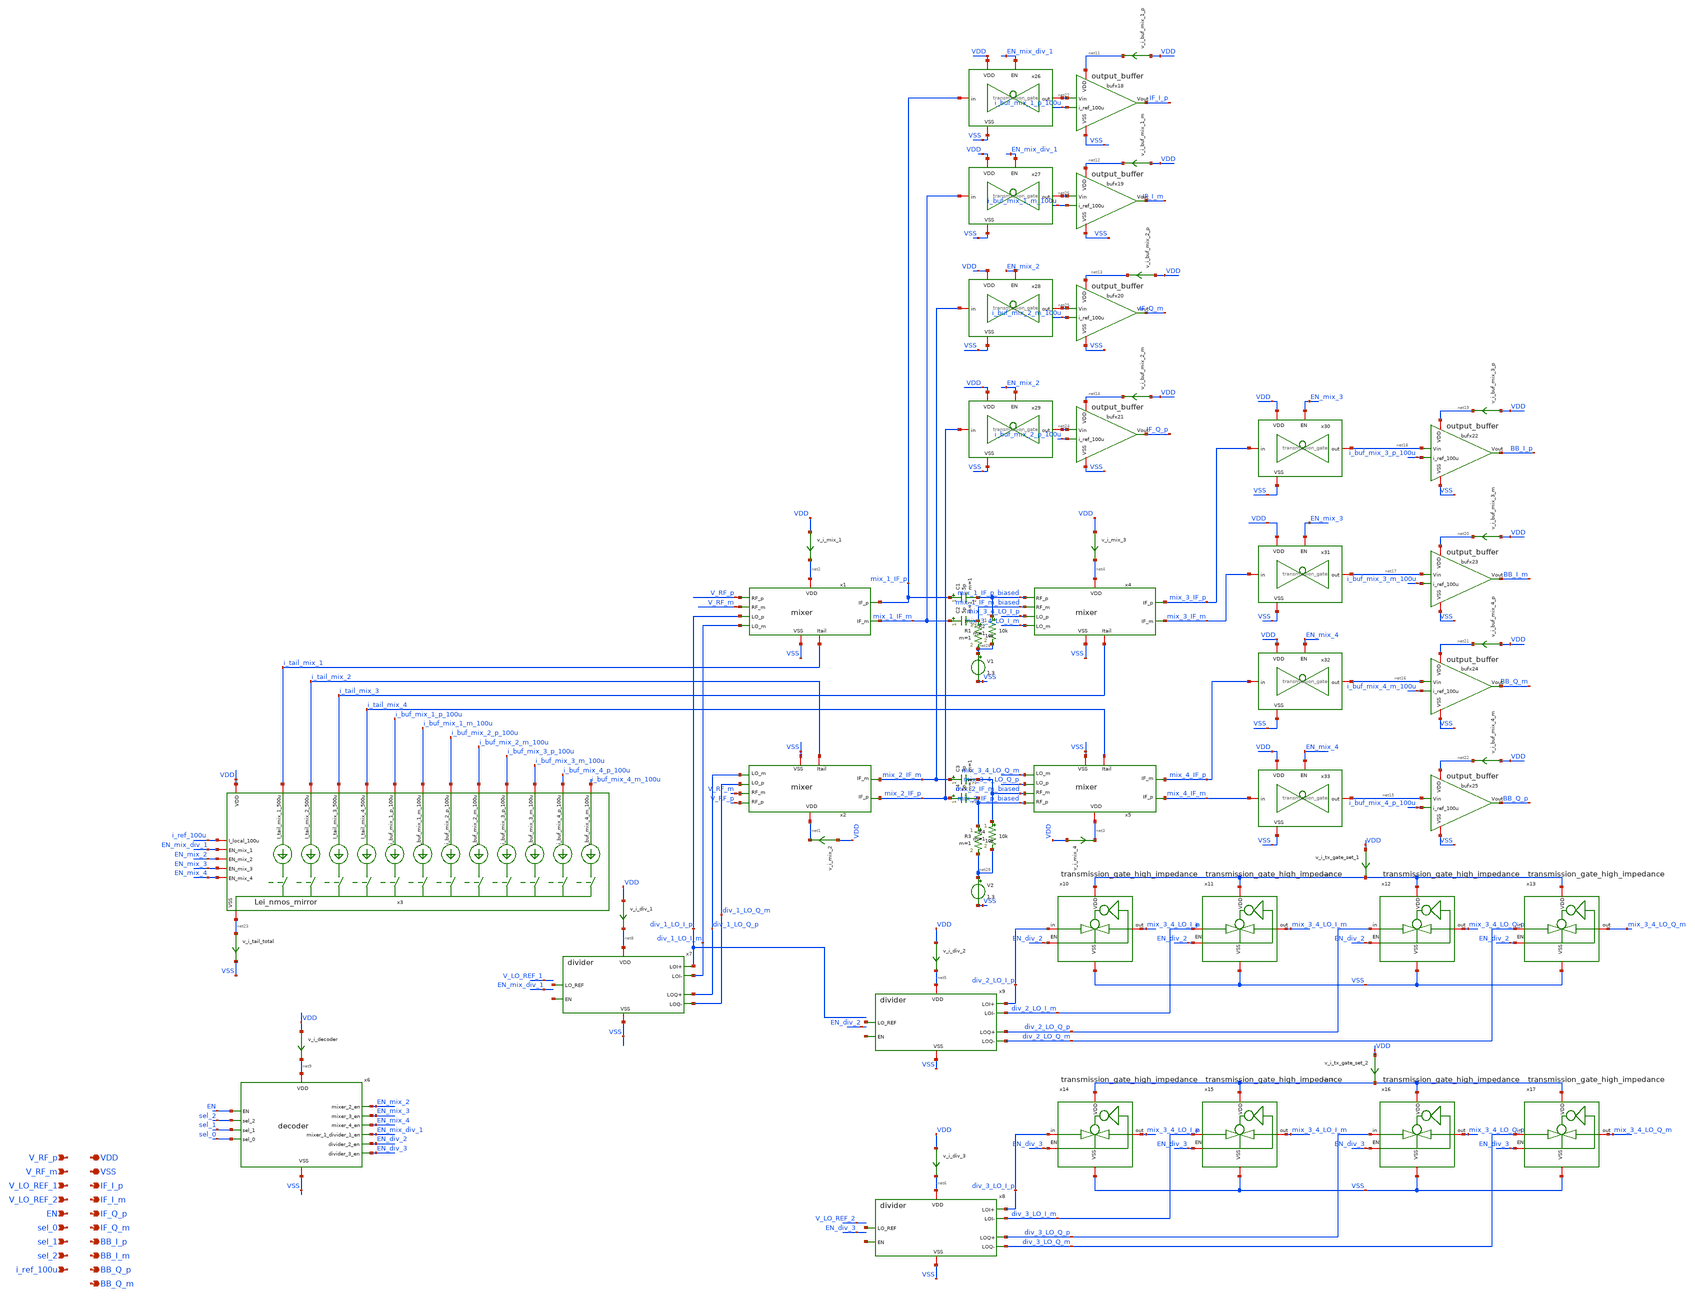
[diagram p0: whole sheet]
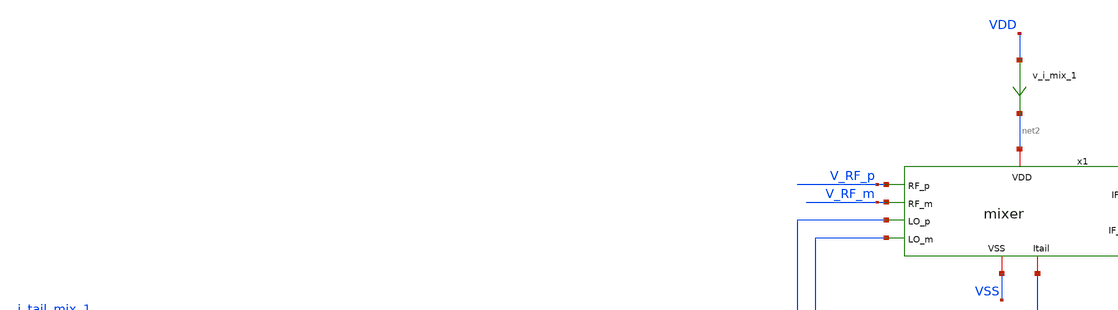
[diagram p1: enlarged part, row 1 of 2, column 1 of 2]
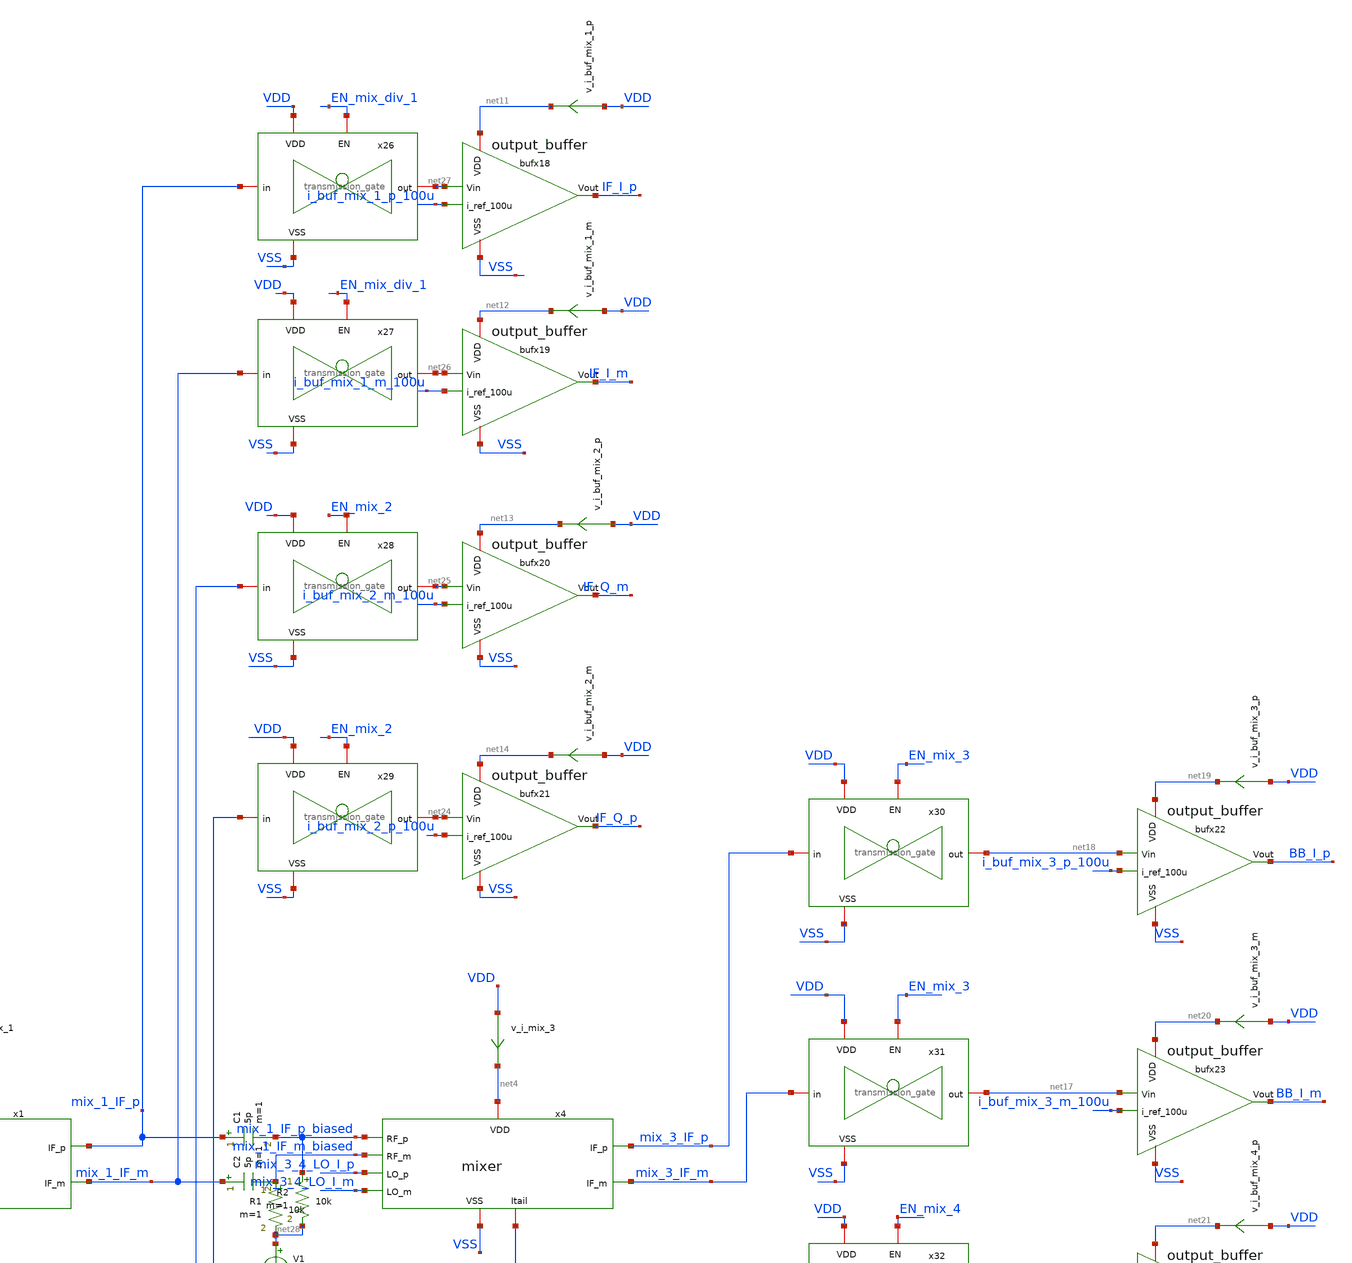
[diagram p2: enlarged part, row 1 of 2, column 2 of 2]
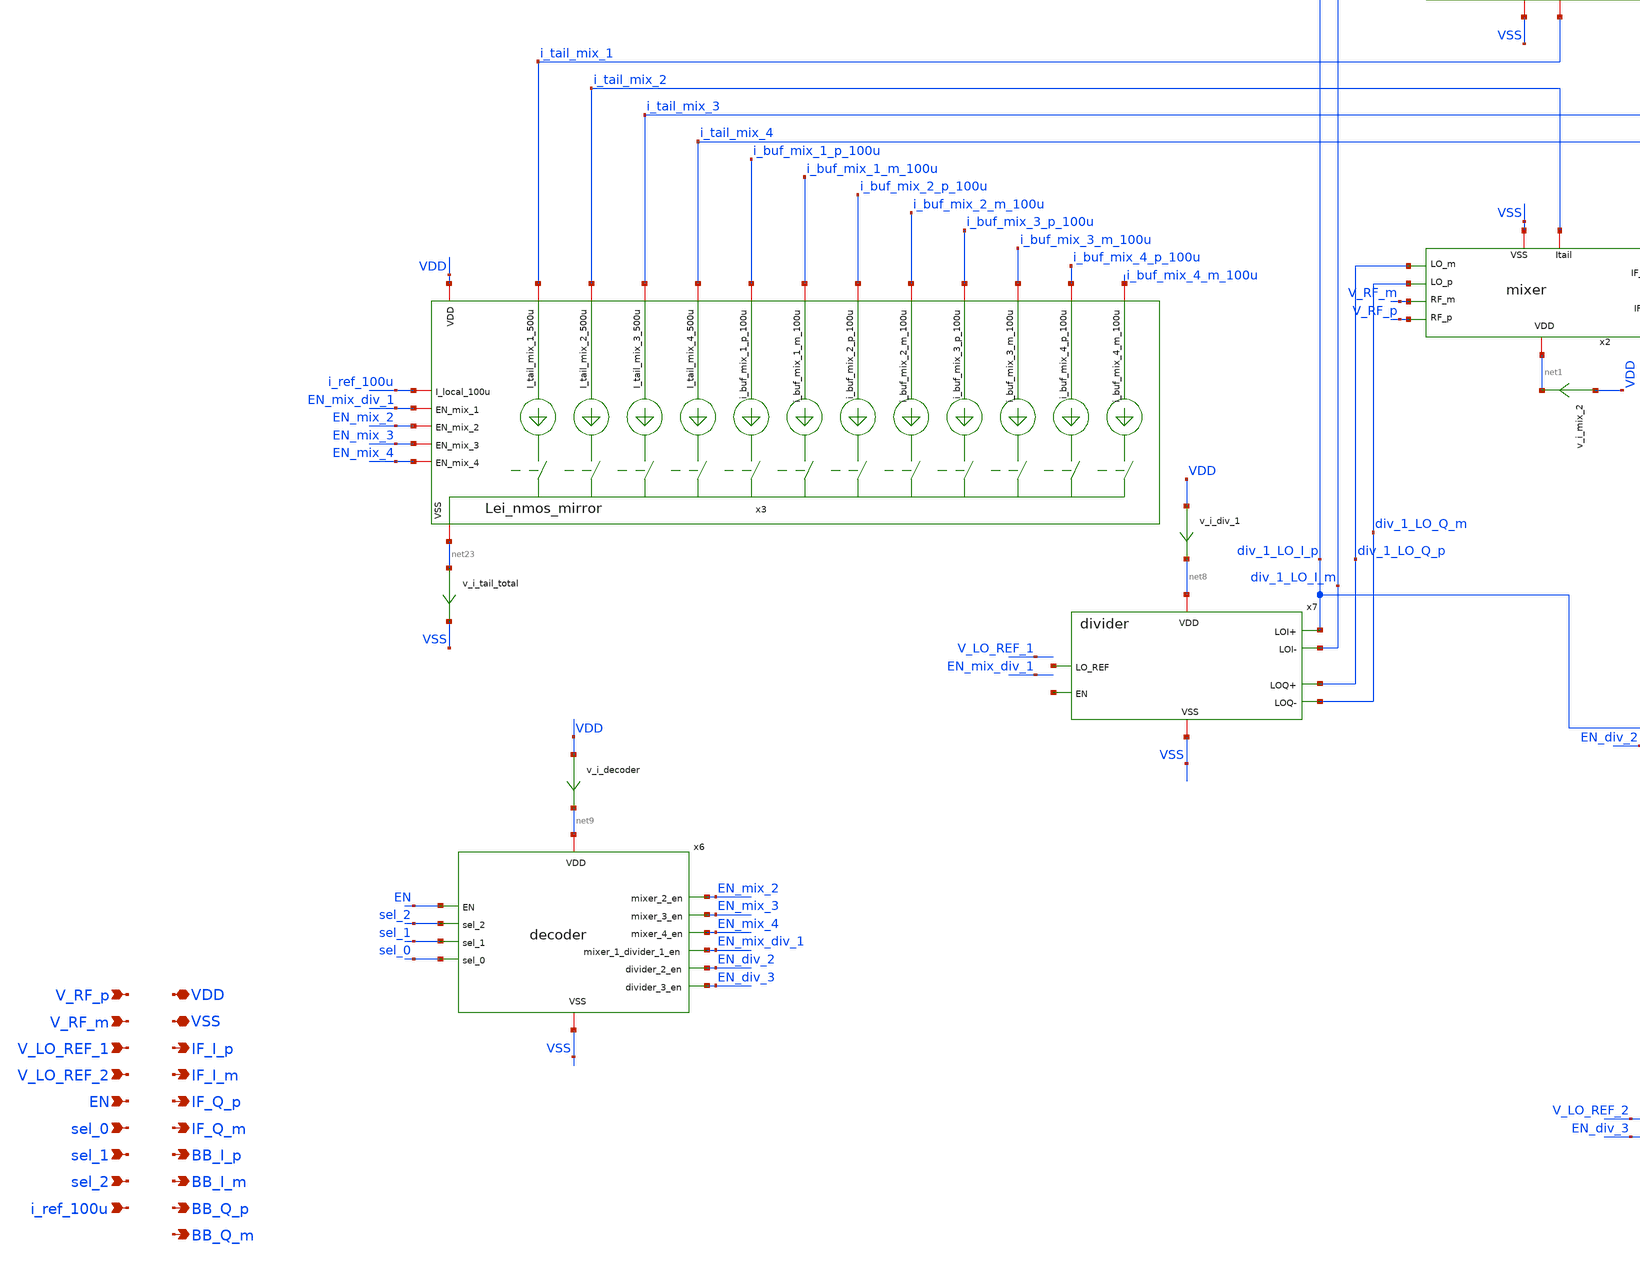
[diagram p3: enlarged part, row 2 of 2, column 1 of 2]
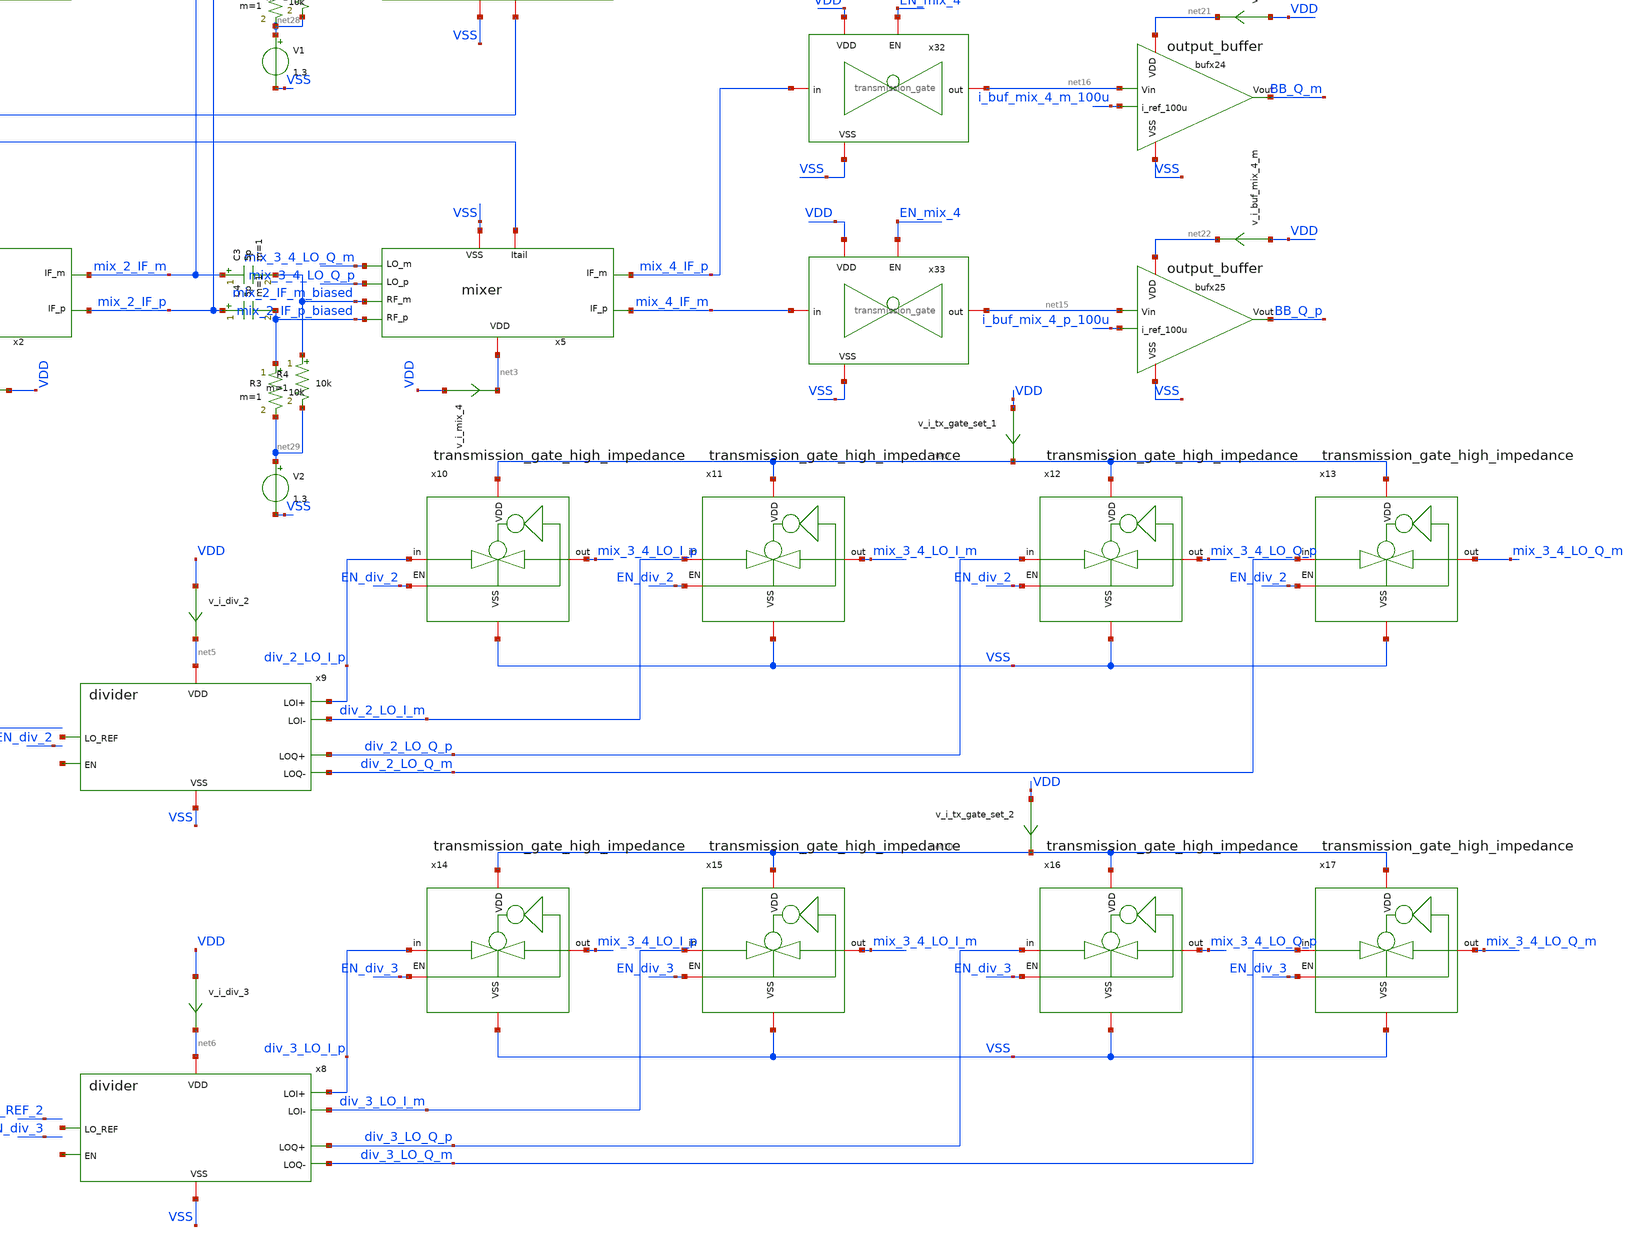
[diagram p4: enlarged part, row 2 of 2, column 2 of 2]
** sch_path: designs/top_level/schematic/top.sch
**.subckt top VDD VSS V_RF_p V_RF_m V_LO_REF_1 V_LO_REF_2 EN sel_0 sel_1 sel_2 i_ref_100u IF_I_p
*+ IF_I_m IF_Q_p IF_Q_m BB_I_p BB_I_m BB_Q_p BB_Q_m
*.iopin VDD
*.iopin VSS
*.ipin V_RF_p
*.ipin V_RF_m
*.ipin V_LO_REF_1
*.ipin V_LO_REF_2
*.ipin EN
*.ipin sel_0
*.ipin sel_1
*.ipin sel_2
*.ipin i_ref_100u
*.opin IF_I_p
*.opin IF_I_m
*.opin IF_Q_p
*.opin IF_Q_m
*.opin BB_I_p
*.opin BB_I_m
*.opin BB_Q_p
*.opin BB_Q_m
x1 mix_1_IF_p V_RF_p net2 VSS mix_1_IF_m V_RF_m div_1_LO_I_p i_tail_mix_1 div_1_LO_I_m mixer
x2 mix_2_IF_p V_RF_p net1 VSS mix_2_IF_m V_RF_m div_1_LO_Q_m i_tail_mix_2 div_1_LO_Q_p mixer
x4 mix_3_IF_p mix_1_IF_p_biased net4 VSS mix_3_IF_m mix_1_IF_m_biased mix_3_4_LO_I_p i_tail_mix_3
+ mix_3_4_LO_I_m mixer
x5 mix_4_IF_m mix_2_IF_p_biased net3 VSS mix_4_IF_p mix_2_IF_m_biased mix_3_4_LO_Q_p i_tail_mix_4
+ mix_3_4_LO_Q_m mixer
x6 net9 VSS EN sel_2 EN_mix_2 sel_1 EN_mix_3 EN_mix_4 sel_0 EN_div_2 EN_div_3 EN_mix_div_1 decoder
x7 net8 VSS net30 div_1_LO_I_p div_1_LO_I_m div_1_LO_Q_p div_1_LO_Q_m net31 divider
x8 net6 VSS net32 div_3_LO_I_p div_3_LO_I_m div_3_LO_Q_p div_3_LO_Q_m net33 divider
x9 net5 VSS net34 div_2_LO_I_p div_2_LO_I_m div_2_LO_Q_p div_2_LO_Q_m net35 divider
x10 net7 div_2_LO_I_p mix_3_4_LO_I_p VSS EN_div_2 transmission_gate_high_impedance
x11 net7 div_2_LO_I_m mix_3_4_LO_I_m VSS EN_div_2 transmission_gate_high_impedance
x12 net7 div_2_LO_Q_p mix_3_4_LO_Q_p VSS EN_div_2 transmission_gate_high_impedance
x13 net7 div_2_LO_Q_m mix_3_4_LO_Q_m VSS EN_div_2 transmission_gate_high_impedance
x14 net10 div_3_LO_I_p mix_3_4_LO_I_p VSS EN_div_3 transmission_gate_high_impedance
x15 net10 div_3_LO_I_m mix_3_4_LO_I_m VSS EN_div_3 transmission_gate_high_impedance
x16 net10 div_3_LO_Q_p mix_3_4_LO_Q_p VSS EN_div_3 transmission_gate_high_impedance
x17 net10 div_3_LO_Q_m mix_3_4_LO_Q_m VSS EN_div_3 transmission_gate_high_impedance
x18 IF_I_p net27 i_buf_mix_1_p_100u net11 VSS output_buffer
x19 IF_I_m net26 i_buf_mix_1_m_100u net12 VSS output_buffer
x20 IF_Q_m net25 i_buf_mix_2_m_100u net13 VSS output_buffer
x21 IF_Q_p net24 i_buf_mix_2_p_100u net14 VSS output_buffer
x22 BB_I_p net18 i_buf_mix_3_p_100u net19 VSS output_buffer
x23 BB_I_m net17 i_buf_mix_3_m_100u net20 VSS output_buffer
x24 BB_Q_m net16 i_buf_mix_4_m_100u net21 VSS output_buffer
x25 BB_Q_p net15 i_buf_mix_4_p_100u net22 VSS output_buffer
x3 VDD i_tail_mix_1 EN_mix_div_1 EN_mix_2 EN_mix_3 EN_mix_4 i_tail_mix_2 i_tail_mix_3 i_ref_100u
+ i_tail_mix_4 net23 i_buf_mix_1_p_100u i_buf_mix_1_m_100u i_buf_mix_2_p_100u i_buf_mix_2_m_100u
+ i_buf_mix_3_p_100u i_buf_mix_3_m_100u i_buf_mix_4_p_100u i_buf_mix_4_m_100u Lei_nmos_mirror
v_i_mix_1 VDD net2 0
.save i(v_i_mix_1)
v_i_mix_3 VDD net4 0
.save i(v_i_mix_3)
v_i_mix_4 VDD net3 0
.save i(v_i_mix_4)
v_i_mix_2 VDD net1 0
.save i(v_i_mix_2)
v_i_div_1 VDD net8 0
.save i(v_i_div_1)
v_i_div_2 VDD net5 0
.save i(v_i_div_2)
v_i_div_3 VDD net6 0
.save i(v_i_div_3)
v_i_tail_total net23 VSS 0
.save i(v_i_tail_total)
v_i_buf_mix_1_p VDD net11 0
.save i(v_i_buf_mix_1_p)
v_i_buf_mix_1_m VDD net12 0
.save i(v_i_buf_mix_1_m)
v_i_buf_mix_2_p VDD net13 0
.save i(v_i_buf_mix_2_p)
v_i_buf_mix_2_m VDD net14 0
.save i(v_i_buf_mix_2_m)
v_i_buf_mix_3_p VDD net19 0
.save i(v_i_buf_mix_3_p)
v_i_buf_mix_3_m VDD net20 0
.save i(v_i_buf_mix_3_m)
v_i_buf_mix_4_p VDD net21 0
.save i(v_i_buf_mix_4_p)
v_i_buf_mix_4_m VDD net22 0
.save i(v_i_buf_mix_4_m)
v_i_decoder VDD net9 0
.save i(v_i_decoder)
v_i_tx_gate_set_1 VDD net7 0
.save i(v_i_tx_gate_set_1)
v_i_tx_gate_set_2 VDD net10 0
.save i(v_i_tx_gate_set_2)
x26 EN_mix_div_1 VDD mix_1_IF_p net27 VSS transmission_gate
x27 EN_mix_div_1 VDD mix_1_IF_m net26 VSS transmission_gate
x28 EN_mix_2 VDD mix_2_IF_m net25 VSS transmission_gate
x29 EN_mix_2 VDD mix_2_IF_p net24 VSS transmission_gate
x30 EN_mix_3 VDD mix_3_IF_p net18 VSS transmission_gate
x31 EN_mix_3 VDD mix_3_IF_m net17 VSS transmission_gate
x32 EN_mix_4 VDD mix_4_IF_p net16 VSS transmission_gate
x33 EN_mix_4 VDD mix_4_IF_m net15 VSS transmission_gate
C1 mix_1_IF_p mix_1_IF_p_biased 5p m=1
C2 mix_1_IF_m mix_1_IF_m_biased 5p m=1
V1 net28 VSS 1.3
V2 net29 VSS 1.3
C3 mix_2_IF_m mix_2_IF_m_biased 5p m=1
C4 mix_2_IF_p mix_2_IF_p_biased 5p m=1
R1 mix_1_IF_m_biased net28 10k m=1
R2 mix_1_IF_p_biased net28 10k m=1
R3 mix_2_IF_p_biased net29 10k m=1
R4 mix_2_IF_m_biased net29 10k m=1
**.ends
.end
